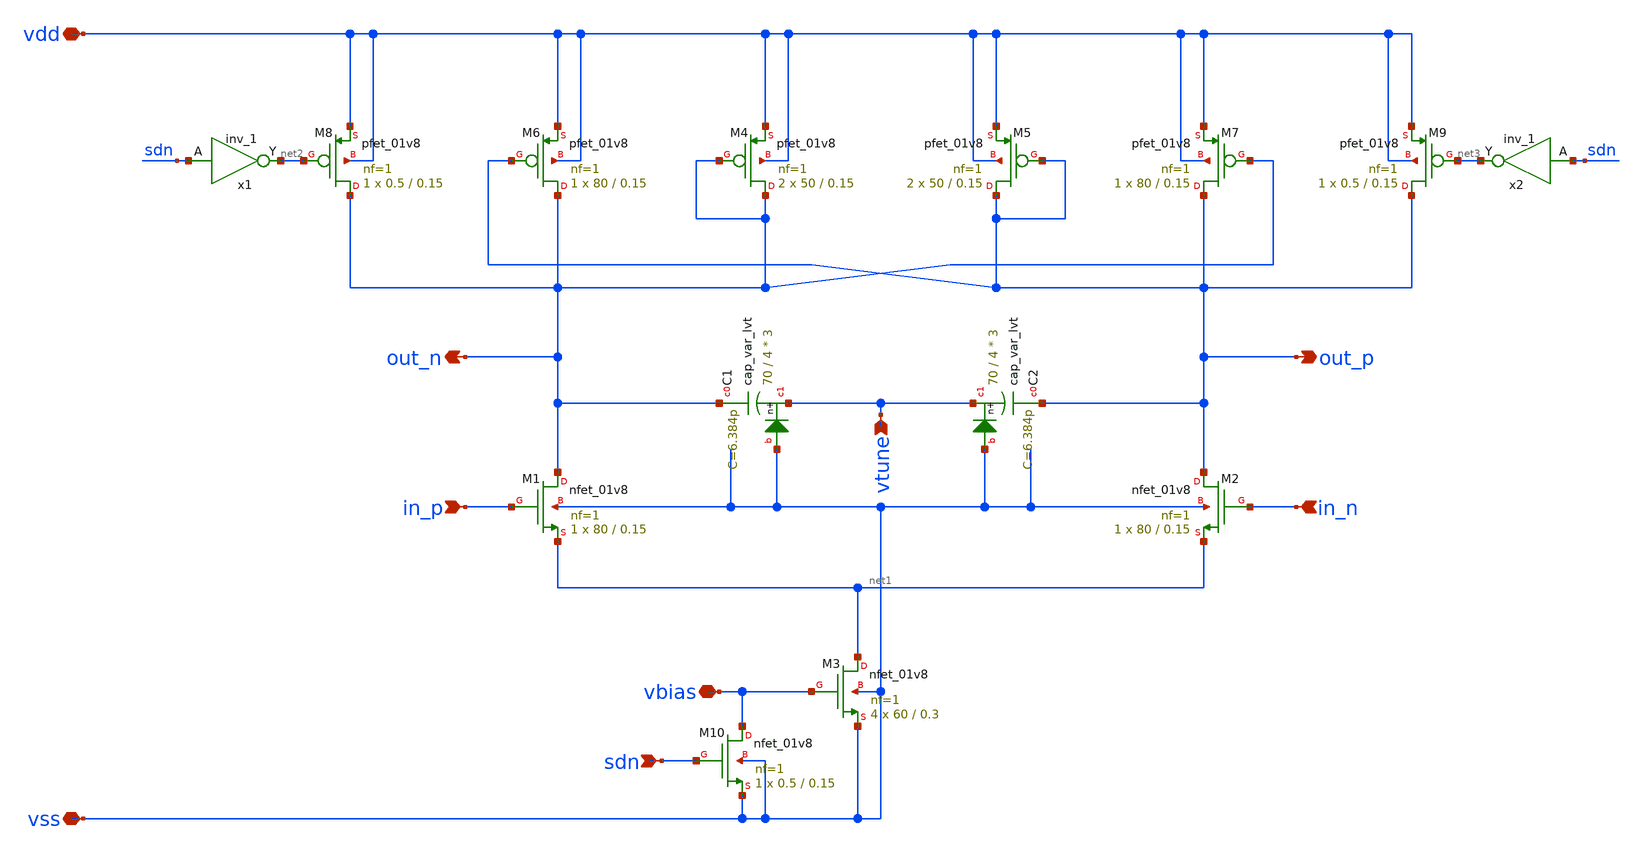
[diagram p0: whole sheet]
** sch_path: pll/pll_vco/xschem/pll_vco_cell_large.sch
**.subckt pll_vco_cell_large vss vdd in_p in_n vbias out_n out_p vtune sdn
*.iopin vss
*.iopin vdd
*.ipin in_p
*.ipin in_n
*.iopin vbias
*.opin out_n
*.opin out_p
*.ipin vtune
*.ipin sdn
XM3 net1 vbias vss vss sky130_fd_pr__nfet_01v8 L=0.3 W=60 nf=1 ad='int((nf+1)/2) * W/nf * 0.29' as='int((nf+2)/2) * W/nf * 0.29'
+ pd='2*int((nf+1)/2) * (W/nf + 0.29)' ps='2*int((nf+2)/2) * (W/nf + 0.29)' nrd='0.29 / W' nrs='0.29 / W'
+ sa=0 sb=0 sd=0 mult=4 m=4
XM10 vbias sdn vss vss sky130_fd_pr__nfet_01v8 L=0.15 W=0.5 nf=1 ad='int((nf+1)/2) * W/nf * 0.29' as='int((nf+2)/2) * W/nf * 0.29'
+ pd='2*int((nf+1)/2) * (W/nf + 0.29)' ps='2*int((nf+2)/2) * (W/nf + 0.29)' nrd='0.29 / W' nrs='0.29 / W'
+ sa=0 sb=0 sd=0 mult=1 m=1
x1 sdn vss vss vdd vdd net2 sky130_fd_sc_hd__inv_1
x2 sdn vss vss vdd vdd net3 sky130_fd_sc_hd__inv_1
XM4 out_n out_n vdd vdd sky130_fd_pr__pfet_01v8 L=0.15 W=50 nf=1 ad='int((nf+1)/2) * W/nf * 0.29' as='int((nf+2)/2) * W/nf * 0.29'
+ pd='2*int((nf+1)/2) * (W/nf + 0.29)' ps='2*int((nf+2)/2) * (W/nf + 0.29)' nrd='0.29 / W' nrs='0.29 / W'
+ sa=0 sb=0 sd=0 mult=2 m=2
XM5 out_p out_p vdd vdd sky130_fd_pr__pfet_01v8 L=0.15 W=50 nf=1 ad='int((nf+1)/2) * W/nf * 0.29' as='int((nf+2)/2) * W/nf * 0.29'
+ pd='2*int((nf+1)/2) * (W/nf + 0.29)' ps='2*int((nf+2)/2) * (W/nf + 0.29)' nrd='0.29 / W' nrs='0.29 / W'
+ sa=0 sb=0 sd=0 mult=2 m=2
XM7 out_p out_n vdd vdd sky130_fd_pr__pfet_01v8 L=0.15 W=80 nf=1 ad='int((nf+1)/2) * W/nf * 0.29' as='int((nf+2)/2) * W/nf * 0.29'
+ pd='2*int((nf+1)/2) * (W/nf + 0.29)' ps='2*int((nf+2)/2) * (W/nf + 0.29)' nrd='0.29 / W' nrs='0.29 / W'
+ sa=0 sb=0 sd=0 mult=1 m=1
XM6 out_n out_p vdd vdd sky130_fd_pr__pfet_01v8 L=0.15 W=80 nf=1 ad='int((nf+1)/2) * W/nf * 0.29' as='int((nf+2)/2) * W/nf * 0.29'
+ pd='2*int((nf+1)/2) * (W/nf + 0.29)' ps='2*int((nf+2)/2) * (W/nf + 0.29)' nrd='0.29 / W' nrs='0.29 / W'
+ sa=0 sb=0 sd=0 mult=1 m=1
XM8 out_n net2 vdd vdd sky130_fd_pr__pfet_01v8 L=0.15 W=0.5 nf=1 ad='int((nf+1)/2) * W/nf * 0.29' as='int((nf+2)/2) * W/nf * 0.29'
+ pd='2*int((nf+1)/2) * (W/nf + 0.29)' ps='2*int((nf+2)/2) * (W/nf + 0.29)' nrd='0.29 / W' nrs='0.29 / W'
+ sa=0 sb=0 sd=0 mult=1 m=1
XM9 out_p net3 vdd vdd sky130_fd_pr__pfet_01v8 L=0.15 W=0.5 nf=1 ad='int((nf+1)/2) * W/nf * 0.29' as='int((nf+2)/2) * W/nf * 0.29'
+ pd='2*int((nf+1)/2) * (W/nf + 0.29)' ps='2*int((nf+2)/2) * (W/nf + 0.29)' nrd='0.29 / W' nrs='0.29 / W'
+ sa=0 sb=0 sd=0 mult=1 m=1
XM1 out_n in_p net1 vss sky130_fd_pr__nfet_01v8 L=0.15 W=80 nf=1 ad='int((nf+1)/2) * W/nf * 0.29' as='int((nf+2)/2) * W/nf * 0.29'
+ pd='2*int((nf+1)/2) * (W/nf + 0.29)' ps='2*int((nf+2)/2) * (W/nf + 0.29)' nrd='0.29 / W' nrs='0.29 / W'
+ sa=0 sb=0 sd=0 mult=1 m=1
XM2 out_p in_n net1 vss sky130_fd_pr__nfet_01v8 L=0.15 W=80 nf=1 ad='int((nf+1)/2) * W/nf * 0.29' as='int((nf+2)/2) * W/nf * 0.29'
+ pd='2*int((nf+1)/2) * (W/nf + 0.29)' ps='2*int((nf+2)/2) * (W/nf + 0.29)' nrd='0.29 / W' nrs='0.29 / W'
+ sa=0 sb=0 sd=0 mult=1 m=1
XC1 out_n vtune vss sky130_fd_pr__cap_var_lvt W=70 L=4 VM=3 m=3
XC2 out_p vtune vss sky130_fd_pr__cap_var_lvt W=70 L=4 VM=3 m=3
**** begin user architecture code


*.control
*save i(@m.${path}xm1.msky130_fd_pr__nfet_01v8[id])
*save @m.${path}xm1.msky130_fd_pr__nfet_01v8[gm]
*save v(@m.${path}xm1.msky130_fd_pr__nfet_01v8[vds])
*save v(@m.${path}xm1.msky130_fd_pr__nfet_01v8[vgs])
*save v(@m.${path}xm1.msky130_fd_pr__nfet_01v8[vth])
*save v(@m.${path}xm1.msky130_fd_pr__nfet_01v8[vdsat])

*save i(@m.${path}xm2.msky130_fd_pr__nfet_01v8[id])
*save @m.${path}xm2.msky130_fd_pr__nfet_01v8[gm]
*save v(@m.${path}xm2.msky130_fd_pr__nfet_01v8[vds])
*save v(@m.${path}xm2.msky130_fd_pr__nfet_01v8[vgs])
*save v(@m.${path}xm2.msky130_fd_pr__nfet_01v8[vth])
*save v(@m.${path}xm2.msky130_fd_pr__nfet_01v8[vdsat])
*.endc


**** end user architecture code
**.ends
.end
